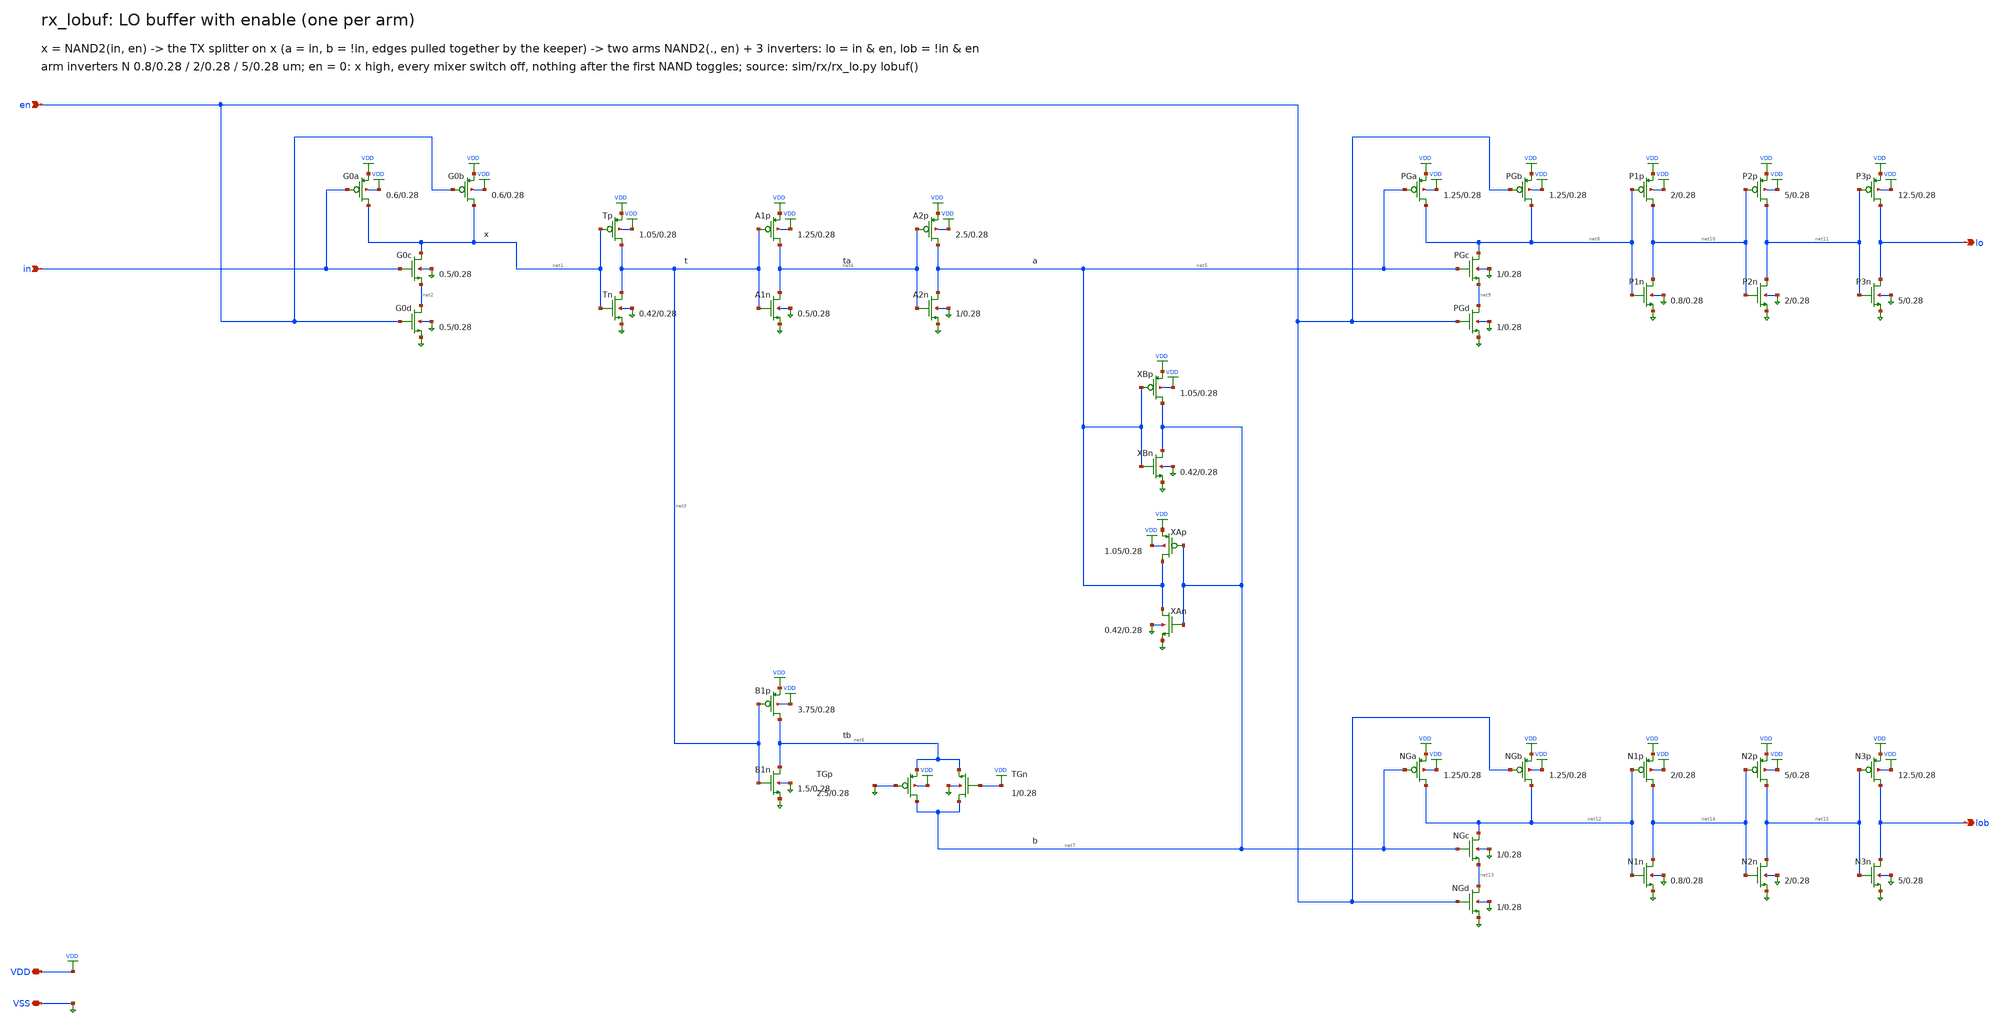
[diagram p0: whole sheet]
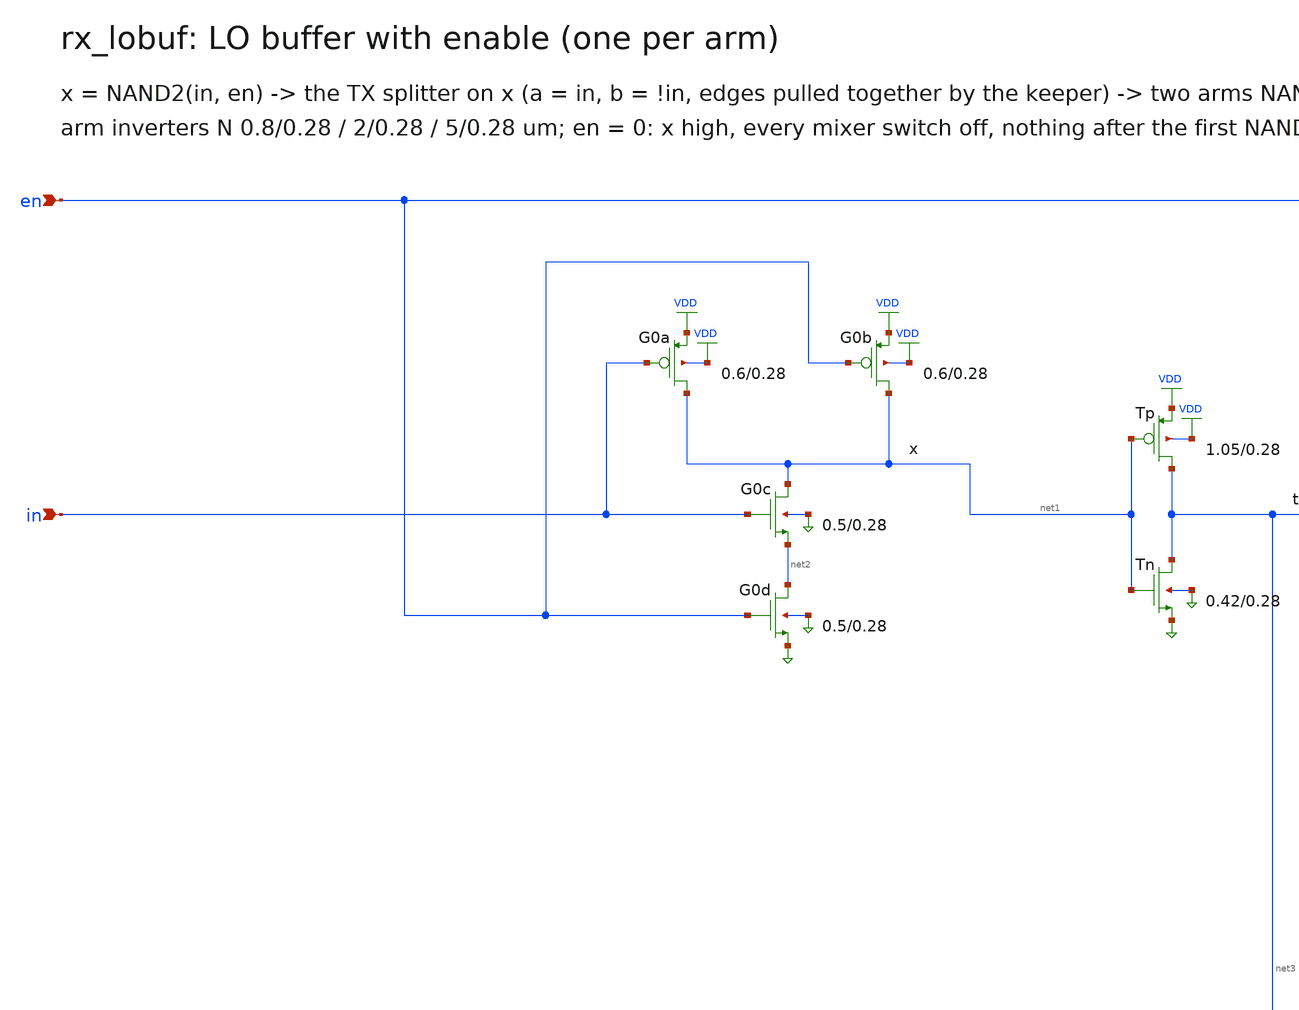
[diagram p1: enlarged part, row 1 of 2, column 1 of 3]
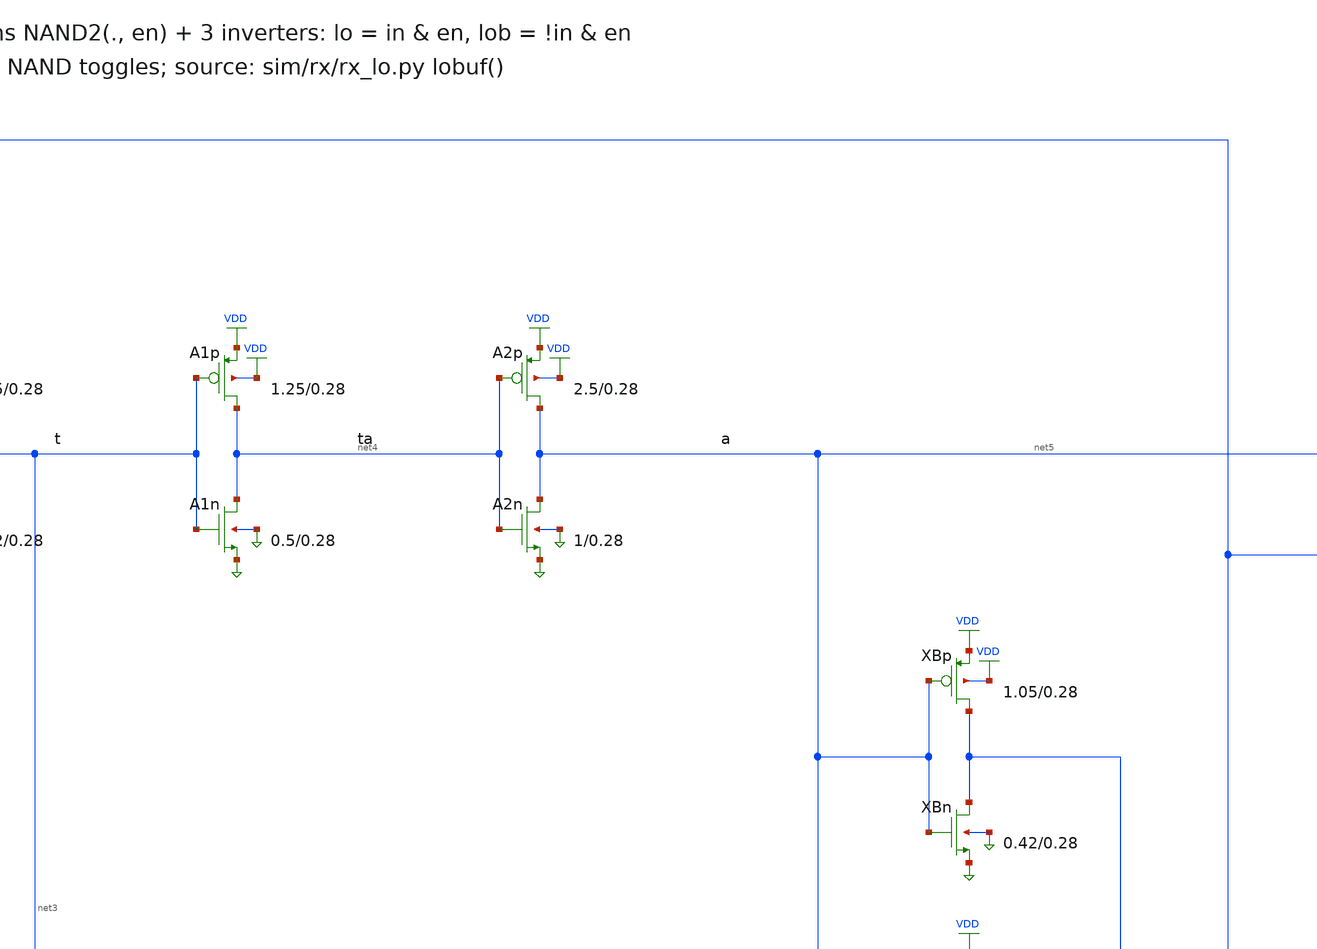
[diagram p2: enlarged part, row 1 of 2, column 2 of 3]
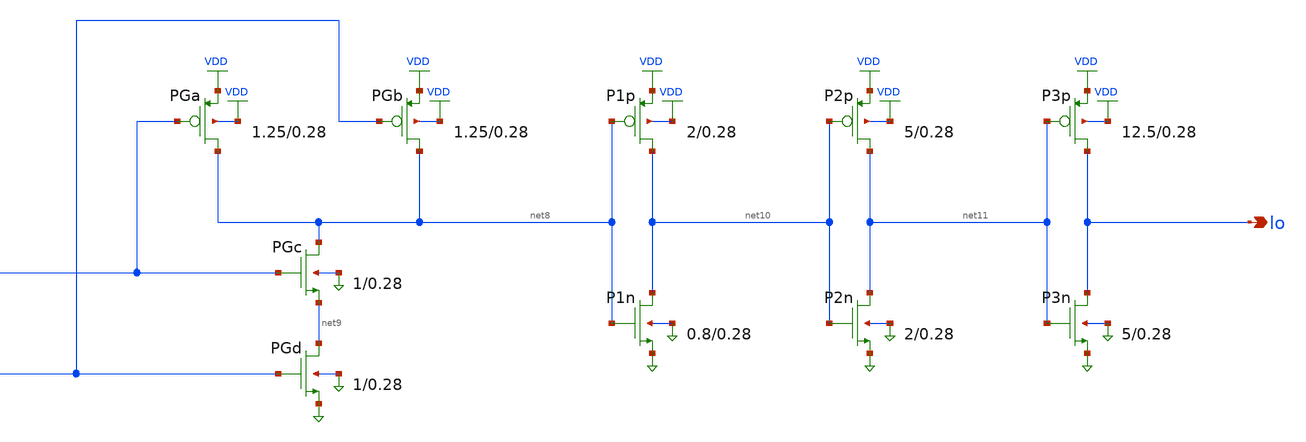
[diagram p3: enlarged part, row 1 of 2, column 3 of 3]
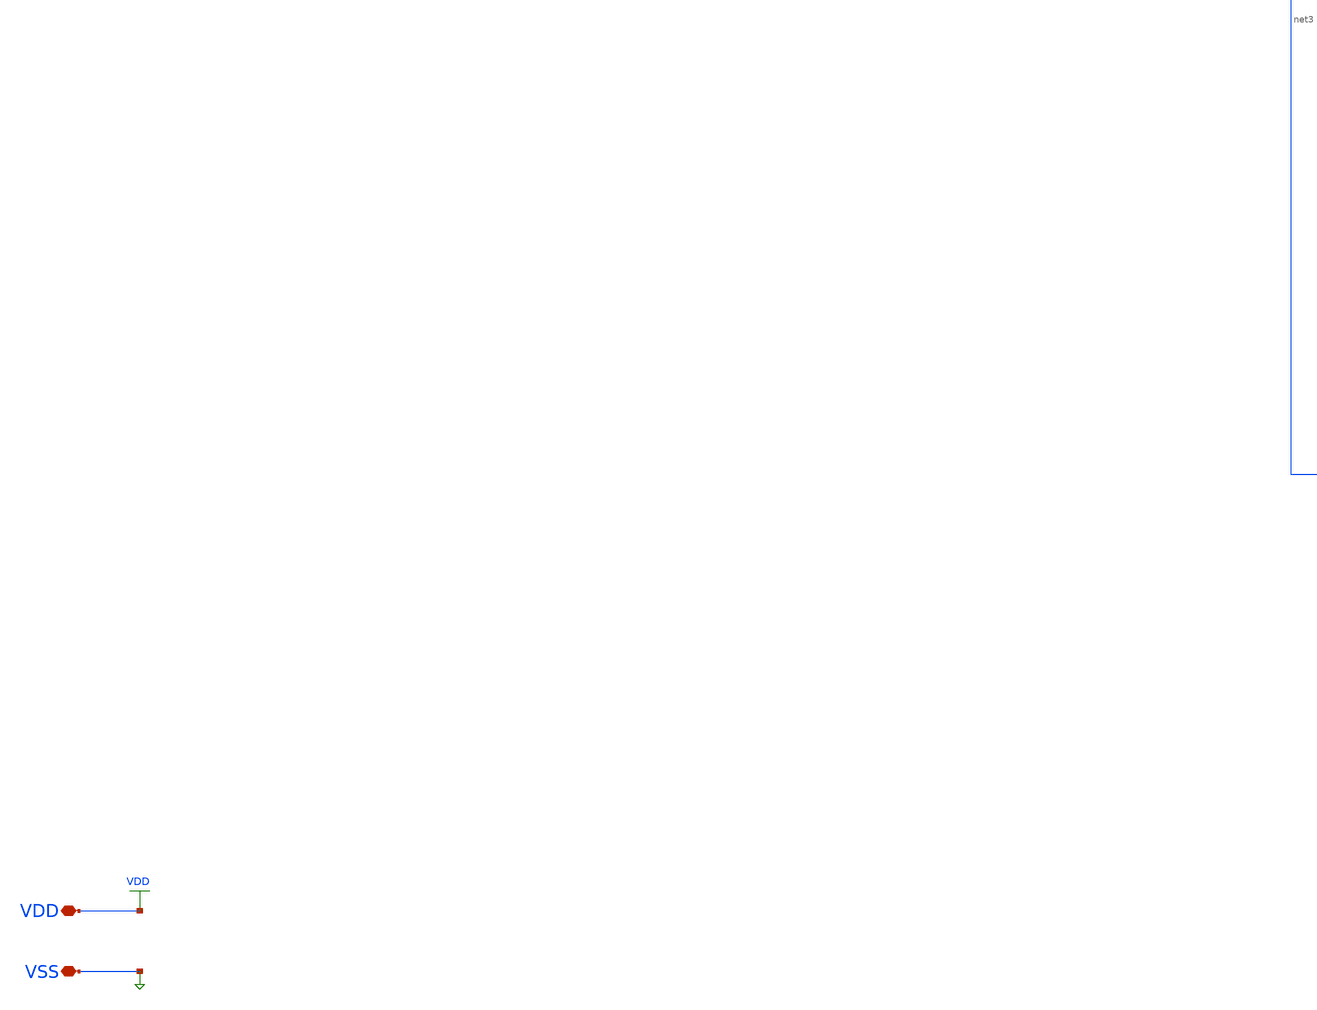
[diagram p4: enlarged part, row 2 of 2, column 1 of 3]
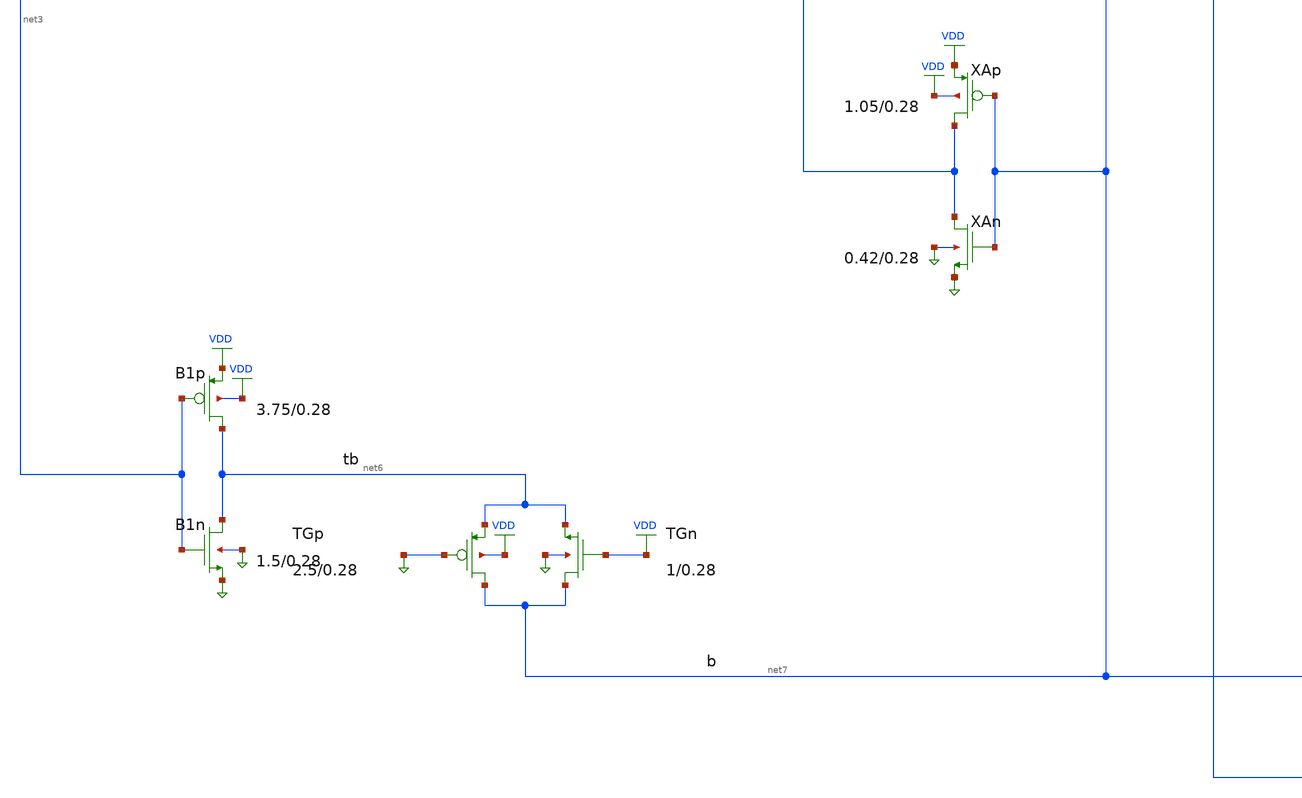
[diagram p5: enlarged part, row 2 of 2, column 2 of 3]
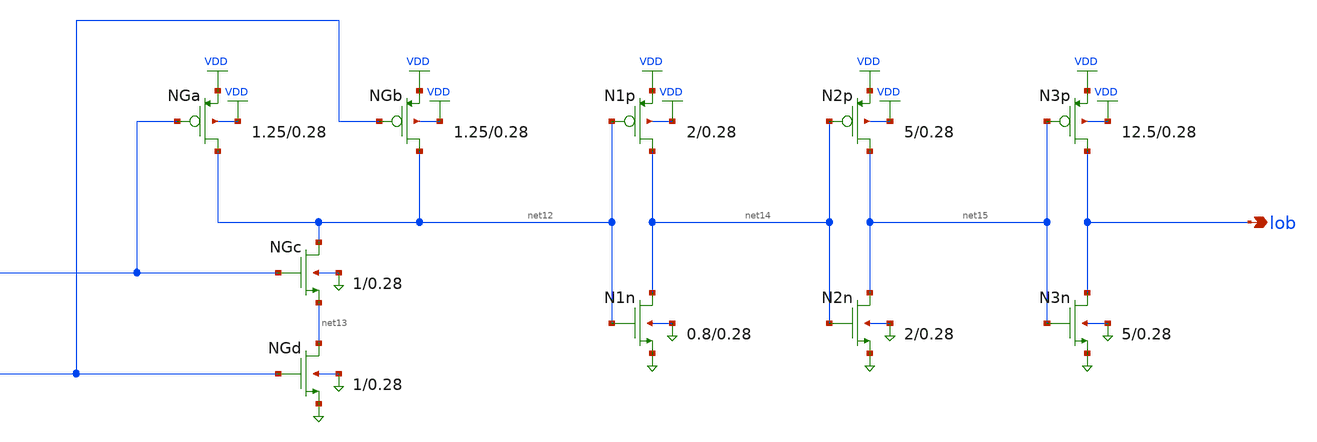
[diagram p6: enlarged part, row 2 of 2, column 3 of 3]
** sch_path: xschem/rx_lobuf.sch
**.subckt rx_lobuf VDD VSS in en lo lob
*.iopin VDD
*.iopin VSS
*.ipin in
*.ipin en
*.opin lo
*.opin lob
XG0a net1 in VDD VDD pfet_03v3 L=0.28u W=0.6u nf=1 ad=0.3p as=0.3p pd=2.2u ps=2.2u nrd=0 nrs=0 sa=0
+ sb=0 sd=0 m=1
XG0b net1 en VDD VDD pfet_03v3 L=0.28u W=0.6u nf=1 ad=0.3p as=0.3p pd=2.2u ps=2.2u nrd=0 nrs=0 sa=0
+ sb=0 sd=0 m=1
XG0c net1 in net2 VSS nfet_03v3 L=0.28u W=0.5u nf=1 ad=0.25p as=0.25p pd=2.0u ps=2.0u nrd=0 nrs=0
+ sa=0 sb=0 sd=0 m=1
XG0d net2 en VSS VSS nfet_03v3 L=0.28u W=0.5u nf=1 ad=0.25p as=0.25p pd=2.0u ps=2.0u nrd=0 nrs=0
+ sa=0 sb=0 sd=0 m=1
XTp net3 net1 VDD VDD pfet_03v3 L=0.28u W=1.0499999999999998u nf=1 ad=0.5249999999999999p
+ as=0.5249999999999999p pd=3.0999999999999996u ps=3.0999999999999996u nrd=0 nrs=0 sa=0 sb=0 sd=0 m=1
XTn net3 net1 VSS VSS nfet_03v3 L=0.28u W=0.41999999999999993u nf=1 ad=0.20999999999999996p
+ as=0.20999999999999996p pd=1.8399999999999999u ps=1.8399999999999999u nrd=0 nrs=0 sa=0 sb=0 sd=0 m=1
XA1p net4 net3 VDD VDD pfet_03v3 L=0.28u W=1.25u nf=1 ad=0.625p as=0.625p pd=3.5u ps=3.5u nrd=0
+ nrs=0 sa=0 sb=0 sd=0 m=1
XA1n net4 net3 VSS VSS nfet_03v3 L=0.28u W=0.5u nf=1 ad=0.25p as=0.25p pd=2.0u ps=2.0u nrd=0 nrs=0
+ sa=0 sb=0 sd=0 m=1
XA2p net5 net4 VDD VDD pfet_03v3 L=0.28u W=2.5u nf=1 ad=1.25p as=1.25p pd=6.0u ps=6.0u nrd=0 nrs=0
+ sa=0 sb=0 sd=0 m=1
XA2n net5 net4 VSS VSS nfet_03v3 L=0.28u W=1.0u nf=1 ad=0.5p as=0.5p pd=3.0u ps=3.0u nrd=0 nrs=0
+ sa=0 sb=0 sd=0 m=1
XB1p net6 net3 VDD VDD pfet_03v3 L=0.28u W=3.7499999999999996u nf=1 ad=1.8749999999999998p
+ as=1.8749999999999998p pd=8.5u ps=8.5u nrd=0 nrs=0 sa=0 sb=0 sd=0 m=1
XB1n net6 net3 VSS VSS nfet_03v3 L=0.28u W=1.5u nf=1 ad=0.75p as=0.75p pd=4.0u ps=4.0u nrd=0 nrs=0
+ sa=0 sb=0 sd=0 m=1
XTGp net7 VSS net6 VDD pfet_03v3 L=0.28u W=2.5u nf=1 ad=1.25p as=1.25p pd=6.0u ps=6.0u nrd=0 nrs=0
+ sa=0 sb=0 sd=0 m=1
XTGn net7 VDD net6 VSS nfet_03v3 L=0.28u W=1.0u nf=1 ad=0.5p as=0.5p pd=3.0u ps=3.0u nrd=0 nrs=0
+ sa=0 sb=0 sd=0 m=1
XXBp net7 net5 VDD VDD pfet_03v3 L=0.28u W=1.0499999999999998u nf=1 ad=0.5249999999999999p
+ as=0.5249999999999999p pd=3.0999999999999996u ps=3.0999999999999996u nrd=0 nrs=0 sa=0 sb=0 sd=0 m=1
XXBn net7 net5 VSS VSS nfet_03v3 L=0.28u W=0.41999999999999993u nf=1 ad=0.20999999999999996p
+ as=0.20999999999999996p pd=1.8399999999999999u ps=1.8399999999999999u nrd=0 nrs=0 sa=0 sb=0 sd=0 m=1
XXAp net5 net7 VDD VDD pfet_03v3 L=0.28u W=1.0499999999999998u nf=1 ad=0.5249999999999999p
+ as=0.5249999999999999p pd=3.0999999999999996u ps=3.0999999999999996u nrd=0 nrs=0 sa=0 sb=0 sd=0 m=1
XXAn net5 net7 VSS VSS nfet_03v3 L=0.28u W=0.41999999999999993u nf=1 ad=0.20999999999999996p
+ as=0.20999999999999996p pd=1.8399999999999999u ps=1.8399999999999999u nrd=0 nrs=0 sa=0 sb=0 sd=0 m=1
XPGa net8 net5 VDD VDD pfet_03v3 L=0.28u W=1.25u nf=1 ad=0.625p as=0.625p pd=3.5u ps=3.5u nrd=0
+ nrs=0 sa=0 sb=0 sd=0 m=1
XPGb net8 en VDD VDD pfet_03v3 L=0.28u W=1.25u nf=1 ad=0.625p as=0.625p pd=3.5u ps=3.5u nrd=0 nrs=0
+ sa=0 sb=0 sd=0 m=1
XPGc net8 net5 net9 VSS nfet_03v3 L=0.28u W=1.0u nf=1 ad=0.5p as=0.5p pd=3.0u ps=3.0u nrd=0 nrs=0
+ sa=0 sb=0 sd=0 m=1
XPGd net9 en VSS VSS nfet_03v3 L=0.28u W=1.0u nf=1 ad=0.5p as=0.5p pd=3.0u ps=3.0u nrd=0 nrs=0 sa=0
+ sb=0 sd=0 m=1
XP1p net10 net8 VDD VDD pfet_03v3 L=0.28u W=2.0u nf=1 ad=1.0p as=1.0p pd=5.0u ps=5.0u nrd=0 nrs=0
+ sa=0 sb=0 sd=0 m=1
XP1n net10 net8 VSS VSS nfet_03v3 L=0.28u W=0.7999999999999999u nf=1 ad=0.39999999999999997p
+ as=0.39999999999999997p pd=2.5999999999999996u ps=2.5999999999999996u nrd=0 nrs=0 sa=0 sb=0 sd=0 m=1
XP2p net11 net10 VDD VDD pfet_03v3 L=0.28u W=5.0u nf=1 ad=2.5p as=2.5p pd=11.0u ps=11.0u nrd=0 nrs=0
+ sa=0 sb=0 sd=0 m=1
XP2n net11 net10 VSS VSS nfet_03v3 L=0.28u W=2.0u nf=1 ad=1.0p as=1.0p pd=5.0u ps=5.0u nrd=0 nrs=0
+ sa=0 sb=0 sd=0 m=1
XP3p lo net11 VDD VDD pfet_03v3 L=0.28u W=12.499999999999998u nf=1 ad=6.249999999999999p
+ as=6.249999999999999p pd=25.999999999999996u ps=25.999999999999996u nrd=0 nrs=0 sa=0 sb=0 sd=0 m=1
XP3n lo net11 VSS VSS nfet_03v3 L=0.28u W=5.0u nf=1 ad=2.5p as=2.5p pd=11.0u ps=11.0u nrd=0 nrs=0
+ sa=0 sb=0 sd=0 m=1
XNGa net12 net7 VDD VDD pfet_03v3 L=0.28u W=1.25u nf=1 ad=0.625p as=0.625p pd=3.5u ps=3.5u nrd=0
+ nrs=0 sa=0 sb=0 sd=0 m=1
XNGb net12 en VDD VDD pfet_03v3 L=0.28u W=1.25u nf=1 ad=0.625p as=0.625p pd=3.5u ps=3.5u nrd=0 nrs=0
+ sa=0 sb=0 sd=0 m=1
XNGc net12 net7 net13 VSS nfet_03v3 L=0.28u W=1.0u nf=1 ad=0.5p as=0.5p pd=3.0u ps=3.0u nrd=0 nrs=0
+ sa=0 sb=0 sd=0 m=1
XNGd net13 en VSS VSS nfet_03v3 L=0.28u W=1.0u nf=1 ad=0.5p as=0.5p pd=3.0u ps=3.0u nrd=0 nrs=0 sa=0
+ sb=0 sd=0 m=1
XN1p net14 net12 VDD VDD pfet_03v3 L=0.28u W=2.0u nf=1 ad=1.0p as=1.0p pd=5.0u ps=5.0u nrd=0 nrs=0
+ sa=0 sb=0 sd=0 m=1
XN1n net14 net12 VSS VSS nfet_03v3 L=0.28u W=0.7999999999999999u nf=1 ad=0.39999999999999997p
+ as=0.39999999999999997p pd=2.5999999999999996u ps=2.5999999999999996u nrd=0 nrs=0 sa=0 sb=0 sd=0 m=1
XN2p net15 net14 VDD VDD pfet_03v3 L=0.28u W=5.0u nf=1 ad=2.5p as=2.5p pd=11.0u ps=11.0u nrd=0 nrs=0
+ sa=0 sb=0 sd=0 m=1
XN2n net15 net14 VSS VSS nfet_03v3 L=0.28u W=2.0u nf=1 ad=1.0p as=1.0p pd=5.0u ps=5.0u nrd=0 nrs=0
+ sa=0 sb=0 sd=0 m=1
XN3p lob net15 VDD VDD pfet_03v3 L=0.28u W=12.499999999999998u nf=1 ad=6.249999999999999p
+ as=6.249999999999999p pd=25.999999999999996u ps=25.999999999999996u nrd=0 nrs=0 sa=0 sb=0 sd=0 m=1
XN3n lob net15 VSS VSS nfet_03v3 L=0.28u W=5.0u nf=1 ad=2.5p as=2.5p pd=11.0u ps=11.0u nrd=0 nrs=0
+ sa=0 sb=0 sd=0 m=1
**.ends
.end
